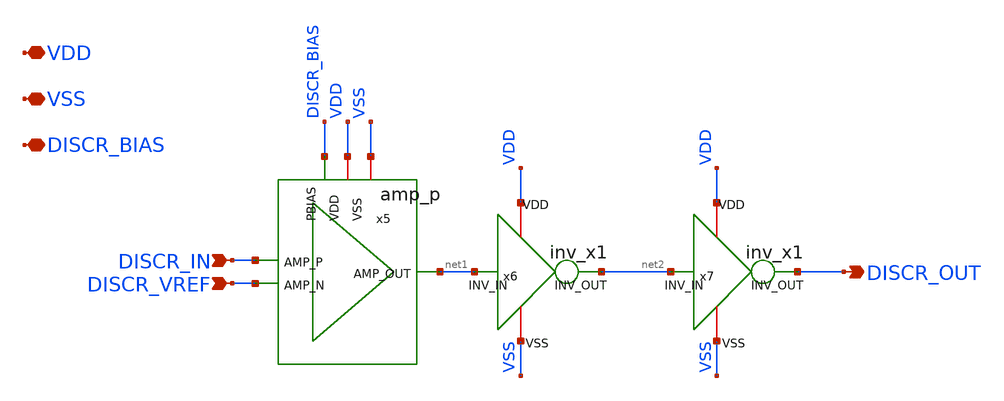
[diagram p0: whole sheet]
** sch_path: xschem/pdiscr.sch
**.subckt pdiscr VDD VSS DISCR_IN DISCR_VREF DISCR_OUT DISCR_BIAS
*.iopin VDD
*.iopin VSS
*.ipin DISCR_IN
*.ipin DISCR_VREF
*.opin DISCR_OUT
*.iopin DISCR_BIAS
x6 VDD VSS net2 net1 inv_x1
x7 VDD VSS DISCR_OUT net2 inv_x1
x5 VDD VSS net1 DISCR_IN DISCR_VREF DISCR_BIAS amp_p
**.ends

* expanding   symbol:  inv_x1.sym # of pins=4
** sym_path: xschem/inv_x1.sym
** sch_path: xschem/inv_x1.sch
.subckt inv_x1 VDD VSS INV_OUT INV_IN
*.ipin INV_IN
*.opin INV_OUT
*.iopin VDD
*.iopin VSS
XM3 INV_OUT INV_IN VDD VDD sky130_fd_pr__pfet_01v8 L=0.15 W=1 nf=1 ad='int((nf+1)/2) * W/nf * 0.29' as='int((nf+2)/2) * W/nf * 0.29'
+ pd='2*int((nf+1)/2) * (W/nf + 0.29)' ps='2*int((nf+2)/2) * (W/nf + 0.29)' nrd='0.29 / W' nrs='0.29 / W'
+ sa=0 sb=0 sd=0 mult=1 m=1
XM5 INV_OUT INV_IN VSS VSS sky130_fd_pr__nfet_01v8 L=0.15 W=1 nf=1 ad='int((nf+1)/2) * W/nf * 0.29' as='int((nf+2)/2) * W/nf * 0.29'
+ pd='2*int((nf+1)/2) * (W/nf + 0.29)' ps='2*int((nf+2)/2) * (W/nf + 0.29)' nrd='0.29 / W' nrs='0.29 / W'
+ sa=0 sb=0 sd=0 mult=1 m=1
.ends


* expanding   symbol:  amp_p.sym # of pins=6
** sym_path: xschem/amp_p.sym
** sch_path: xschem/amp_p.sch
.subckt amp_p VDD VSS AMP_OUT AMP_P AMP_N PBIAS
*.ipin AMP_P
*.ipin AMP_N
*.opin AMP_OUT
*.ipin PBIAS
*.iopin VDD
*.iopin VSS
XM1 VTAIL PBIAS VDD VDD sky130_fd_pr__pfet_01v8 L=1 W=1 nf=1 ad='int((nf+1)/2) * W/nf * 0.29' as='int((nf+2)/2) * W/nf * 0.29'
+ pd='2*int((nf+1)/2) * (W/nf + 0.29)' ps='2*int((nf+2)/2) * (W/nf + 0.29)' nrd='0.29 / W' nrs='0.29 / W'
+ sa=0 sb=0 sd=0 mult=8 m=8
XM2 AMP_OUT VFOLD VSS VSS sky130_fd_pr__nfet_01v8 L=0.15 W=10 nf=1 ad='int((nf+1)/2) * W/nf * 0.29' as='int((nf+2)/2) * W/nf * 0.29'
+ pd='2*int((nf+1)/2) * (W/nf + 0.29)' ps='2*int((nf+2)/2) * (W/nf + 0.29)' nrd='0.29 / W' nrs='0.29 / W'
+ sa=0 sb=0 sd=0 mult=1 m=1
XM6 VFOLD VFOLD VSS VSS sky130_fd_pr__nfet_01v8 L=0.15 W=10 nf=1 ad='int((nf+1)/2) * W/nf * 0.29' as='int((nf+2)/2) * W/nf * 0.29'
+ pd='2*int((nf+1)/2) * (W/nf + 0.29)' ps='2*int((nf+2)/2) * (W/nf + 0.29)' nrd='0.29 / W' nrs='0.29 / W'
+ sa=0 sb=0 sd=0 mult=1 m=1
XM4 AMP_OUT AMP_N VTAIL VDD sky130_fd_pr__pfet_01v8 L=0.15 W=10 nf=2 ad='int((nf+1)/2) * W/nf * 0.29'
+ as='int((nf+2)/2) * W/nf * 0.29' pd='2*int((nf+1)/2) * (W/nf + 0.29)' ps='2*int((nf+2)/2) * (W/nf + 0.29)'
+ nrd='0.29 / W' nrs='0.29 / W' sa=0 sb=0 sd=0 mult=1 m=1
XM5 VFOLD AMP_P VTAIL VDD sky130_fd_pr__pfet_01v8 L=0.15 W=10 nf=2 ad='int((nf+1)/2) * W/nf * 0.29' as='int((nf+2)/2) * W/nf * 0.29'
+ pd='2*int((nf+1)/2) * (W/nf + 0.29)' ps='2*int((nf+2)/2) * (W/nf + 0.29)' nrd='0.29 / W' nrs='0.29 / W'
+ sa=0 sb=0 sd=0 mult=1 m=1
.ends

.end
